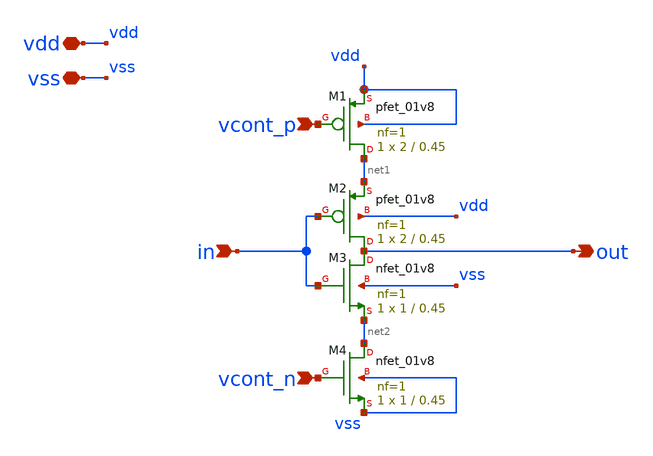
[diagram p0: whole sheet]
** sch_path: xschem/delay_stage.sch
**.subckt delay_stage in out vdd vcont_n vcont_p vss
*.ipin in
*.opin out
*.iopin vdd
*.ipin vcont_n
*.ipin vcont_p
*.iopin vss
XM3 out in net2 vss sky130_fd_pr__nfet_01v8 L=0.45 W=1 nf=1 ad='int((nf+1)/2) * W/nf * 0.29' as='int((nf+2)/2) * W/nf * 0.29'
+ pd='2*int((nf+1)/2) * (W/nf + 0.29)' ps='2*int((nf+2)/2) * (W/nf + 0.29)' nrd='0.29 / W' nrs='0.29 / W'
+ sa=0 sb=0 sd=0 mult=1 m=1
XM2 out in net1 vdd sky130_fd_pr__pfet_01v8 L=0.45 W=2 nf=1 ad='int((nf+1)/2) * W/nf * 0.29' as='int((nf+2)/2) * W/nf * 0.29'
+ pd='2*int((nf+1)/2) * (W/nf + 0.29)' ps='2*int((nf+2)/2) * (W/nf + 0.29)' nrd='0.29 / W' nrs='0.29 / W'
+ sa=0 sb=0 sd=0 mult=1 m=1
XM1 net1 vcont_p vdd vdd sky130_fd_pr__pfet_01v8 L=0.45 W=2 nf=1 ad='int((nf+1)/2) * W/nf * 0.29' as='int((nf+2)/2) * W/nf * 0.29'
+ pd='2*int((nf+1)/2) * (W/nf + 0.29)' ps='2*int((nf+2)/2) * (W/nf + 0.29)' nrd='0.29 / W' nrs='0.29 / W'
+ sa=0 sb=0 sd=0 mult=1 m=1
XM4 net2 vcont_n vss vss sky130_fd_pr__nfet_01v8 L=0.45 W=1 nf=1 ad='int((nf+1)/2) * W/nf * 0.29' as='int((nf+2)/2) * W/nf * 0.29'
+ pd='2*int((nf+1)/2) * (W/nf + 0.29)' ps='2*int((nf+2)/2) * (W/nf + 0.29)' nrd='0.29 / W' nrs='0.29 / W'
+ sa=0 sb=0 sd=0 mult=1 m=1
**.ends
.end
